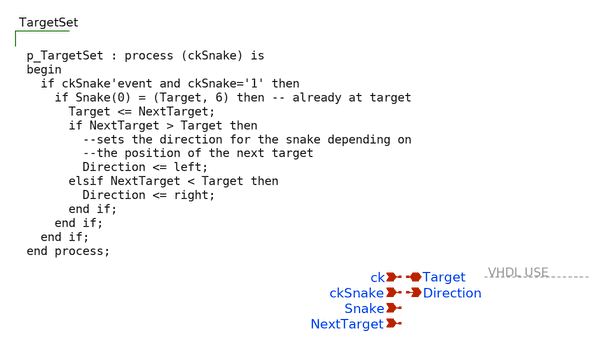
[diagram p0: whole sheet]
** sch_path: xschem/TargetSet.sch
**.subckt TargetSet Snake Direction NextTarget ckSnake ck Target
*.ipin Snake
*.opin Direction
*.ipin NextTarget
*.ipin ckSnake
*.ipin ck
*.iopin Target
**** begin user architecture code


p_TargetSet : process (ckSnake) is
begin
  if ckSnake'event and ckSnake='1' then
    if Snake(0) = (Target, 6) then -- already at target
      Target <= NextTarget;
      if NextTarget > Target then
        --sets the direction for the snake depending on
        --the position of the next target
        Direction <= left;
      elsif NextTarget < Target then
        Direction <= right;
      end if;
    end if;
  end if;
end process;


**** end user architecture code
**.ends
.end
